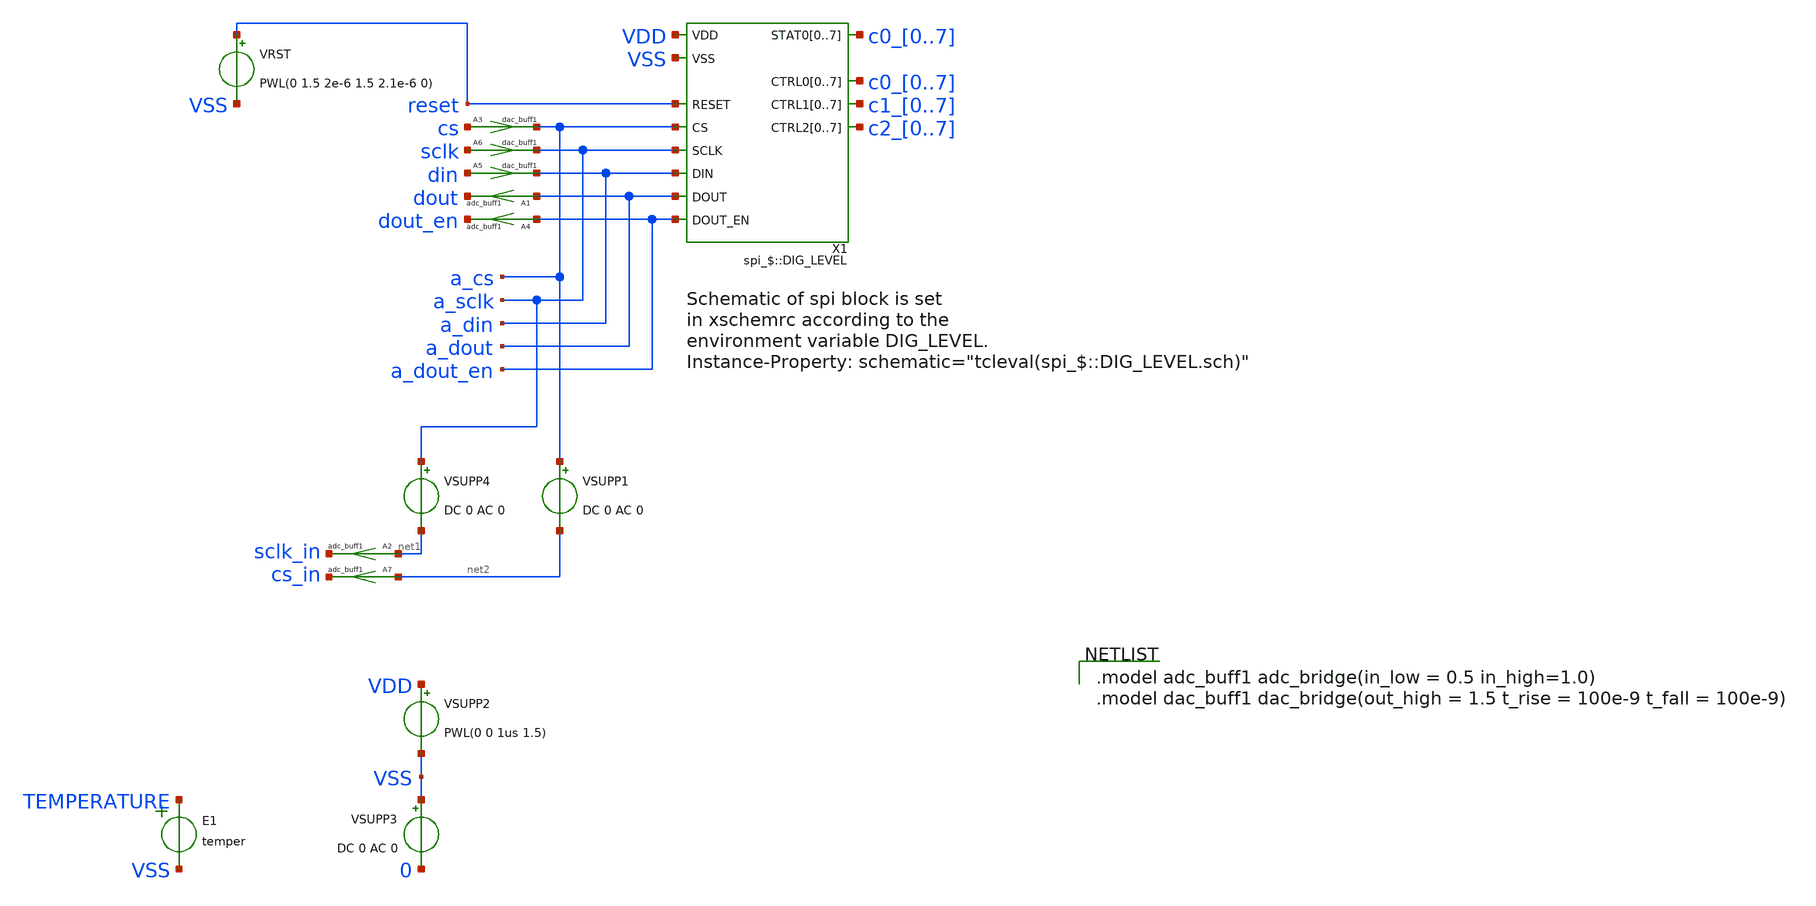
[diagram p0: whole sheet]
** sch_path: ip/spi/xschem/spi_tb.sch
**.subckt spi_tb
A1 [ a_dout ] [ dout ] adc_buff1
A3 [ cs ] [ a_cs ] dac_buff1
A4 [ a_dout_en ] [ dout_en ] adc_buff1
E1 TEMPERATURE VSS VOL=' temper '
VSUPP2 VDD VSS PWL(0 0 1us 1.5)
VSUPP3 VSS 0 DC 0 AC 0
VRST reset VSS PWL(0 1.5 2e-6 1.5 2.1e-6 0)
VSUPP1 a_cs net2 DC 0 AC 0
VSUPP4 a_sclk net1 DC 0 AC 0
A2 [ net1 ] [ sclk_in ] adc_buff1
A7 [ net2 ] [ cs_in ] adc_buff1
A6 [ sclk ] [ a_sclk ] dac_buff1
A5 [ din ] [ a_din ] dac_buff1
X1 a_dout_en reset a_cs c0_0 c0_1 c0_2 c0_3 c0_4 c0_5 c0_6 c0_7 c1_0 c1_1 c1_2 c1_3 c1_4 c1_5 c1_6
+ c1_7 c2_0 c2_1 c2_2 c2_3 c2_4 c2_5 c2_6 c2_7 a_sclk a_din a_dout c0_0 c0_1 c0_2 c0_3 c0_4 c0_5 c0_6 c0_7
+ VDD VSS spi_$::DIG_LEVEL
**** begin user architecture code

.model adc_buff1 adc_bridge(in_low = 0.5 in_high=1.0)
.model dac_buff1 dac_bridge(out_high = 1.5 t_rise = 100e-9 t_fall = 100e-9)


.csparam TB_ID=${::TB_ID}
.csparam MC_RUNS=${::MC_RUNS}
.csparam EXIT_NGSPICE=${::EXIT_NGSPICE}
.lib ${::IHP_MODELS}/sg13g2.lib ${::CORNER}


* this experimental option enables mos model bin
* selection based on W/NF instead of W
.option wnflag=0

.control
****************************************
* cosimulation model
pre_codemodel /home/lukas/git/asictools/ngspice_cm/codemodels/d_mycosim/d_mycosim.cm
****************************************
option savecurrents
* save all



* dummy block for goto
if (1)
if TB_ID = 0
	goto TRAN_TEMP
end
if TB_ID = 1
	goto TRAN_TEMP
end


****************************************
label TRAN_TEMP
* save all
****************************************
if MC_RUNS = 0

	let veclen=3
	let v_avdd = vector(veclen)
	let temp = vector(veclen)
	let run = 0

	*foreach te -40 20 140
	foreach te 20

		.include resources/spi_tran_temp_ops.inc

		reset
		let run = run + 1
	end

	set nobreak
	set width=300
	print v_avdd, temp > sar8_tran_temp.csv

else
	let v_avdd = vector(MC_RUNS)
	let temp = vector(MC_RUNS)
	let run = 0

	set te = 20

	dowhile run < MC_RUNS
		echo MC-RUN: $&run

		.include resources/spi_tran_temp_ops.inc

 		reset
		let run = run + 1
	end

	set nobreak
	set width=300
	print v_avdd, temp > sar8_tran_temp.csv

end
goto done

****************************************
label done
****************************************
if EXIT_NGSPICE > 0.0
	exit
end

end


.endc


.model cosim_m d_mycosim (process_file="/usr/bin/python"
+ process_params=["./resources/spi_stimuli.py", "Baud=9600"])
Acontrol [cs_in sclk_in dout dout_en ] [cs sclk din] cosim_m
**** end user architecture code
**.ends
.end
